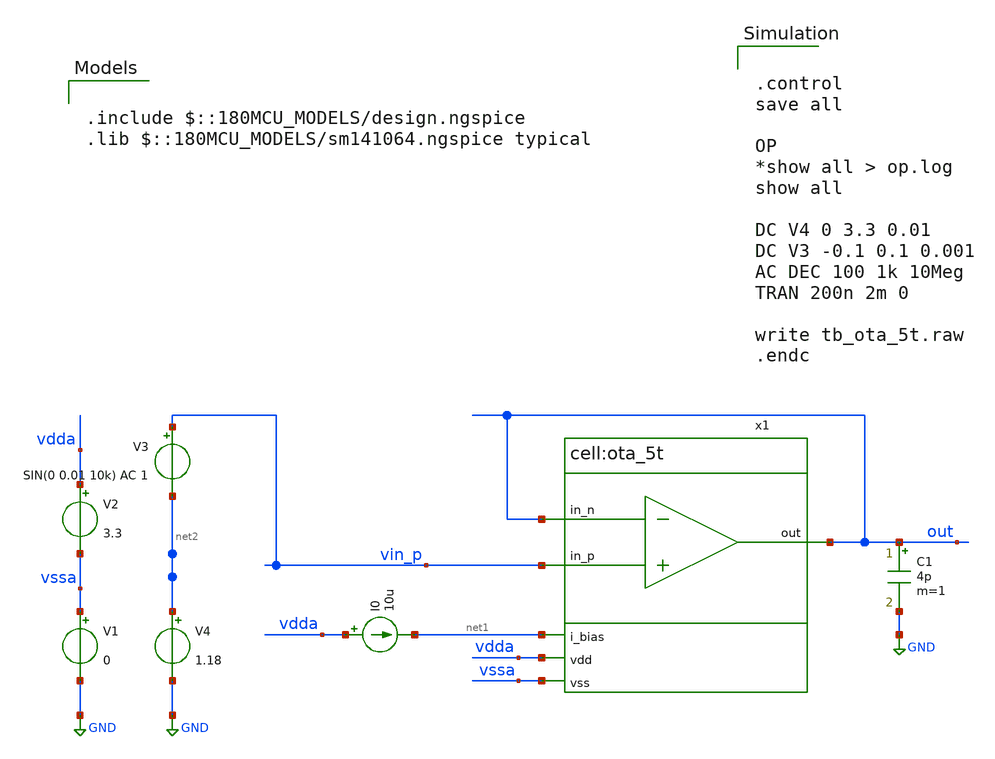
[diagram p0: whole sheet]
** sch_path: designs/switch_matrix_gf180mcu_9t5v0-main/designs/libs/tb_analog/tb_ota_5t_dc/tb_ota_5t_dc.sch
**.subckt tb_ota_5t_dc
V1 vssa GND 0
V2 vdda vssa 3.3
I0 vdda net1 10u
V3 vin_p net2 SIN(0 0.01 10k) AC 1
x1 vdda out vin_p out net1 vssa ota_5t
V4 net2 GND 1.18
C1 out GND 4p m=1
**** begin user architecture code


.control
save all

OP
*show all > op.log
show all

DC V4 0 3.3 0.01
DC V3 -0.1 0.1 0.001
AC DEC 100 1k 10Meg
TRAN 200n 2m 0

write tb_ota_5t.raw
.endc



.include $::180MCU_MODELS/design.ngspice
.lib $::180MCU_MODELS/sm141064.ngspice typical

**** end user architecture code
**.ends
.GLOBAL GND
.end
